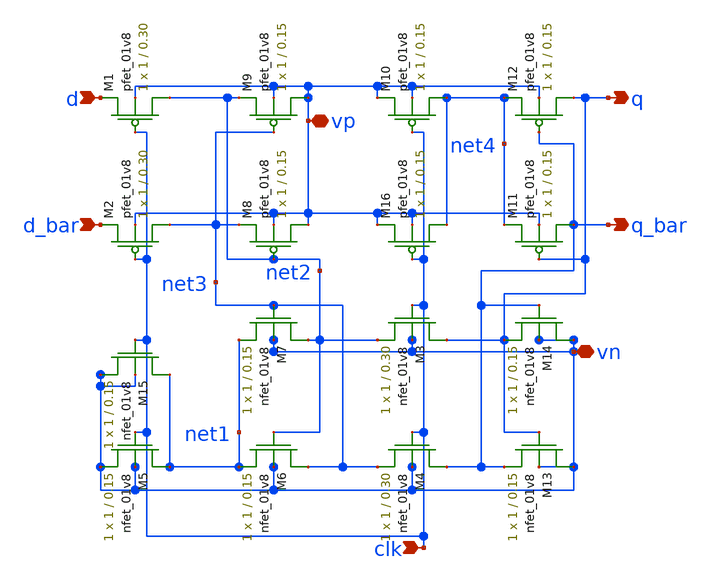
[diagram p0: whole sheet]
** sch_path: xschem/logic_gates/dflipflop.sch
**.subckt dflipflop q q_bar vp vn d_bar d clk
*.opin q
*.opin q_bar
*.iopin vp
*.iopin vn
*.ipin d_bar
*.ipin d
*.ipin clk
XM8 vp net2 net3 vp sky130_fd_pr__pfet_01v8 L=0.15 W=1 nf=1 ad='int((nf+1)/2) * W/nf * 0.29' as='int((nf+2)/2) * W/nf * 0.29'
+ pd='2*int((nf+1)/2) * (W/nf + 0.29)' ps='2*int((nf+2)/2) * (W/nf + 0.29)' nrd='0.29 / W' nrs='0.29 / W'
+ sa=0 sb=0 sd=0 mult=1 m=1
XM9 vp net3 net2 vp sky130_fd_pr__pfet_01v8 L=0.15 W=1 nf=1 ad='int((nf+1)/2) * W/nf * 0.29' as='int((nf+2)/2) * W/nf * 0.29'
+ pd='2*int((nf+1)/2) * (W/nf + 0.29)' ps='2*int((nf+2)/2) * (W/nf + 0.29)' nrd='0.29 / W' nrs='0.29 / W'
+ sa=0 sb=0 sd=0 mult=1 m=1
XM5 net1 clk vn vn sky130_fd_pr__nfet_01v8 L=0.15 W=1 nf=1 ad='int((nf+1)/2) * W/nf * 0.29' as='int((nf+2)/2) * W/nf * 0.29'
+ pd='2*int((nf+1)/2) * (W/nf + 0.29)' ps='2*int((nf+2)/2) * (W/nf + 0.29)' nrd='0.29 / W' nrs='0.29 / W'
+ sa=0 sb=0 sd=0 mult=1 m=1
XM6 net3 net2 net1 vn sky130_fd_pr__nfet_01v8 L=0.15 W=1 nf=1 ad='int((nf+1)/2) * W/nf * 0.29' as='int((nf+2)/2) * W/nf * 0.29'
+ pd='2*int((nf+1)/2) * (W/nf + 0.29)' ps='2*int((nf+2)/2) * (W/nf + 0.29)' nrd='0.29 / W' nrs='0.29 / W'
+ sa=0 sb=0 sd=0 mult=1 m=1
XM7 net2 net3 net1 vn sky130_fd_pr__nfet_01v8 L=0.15 W=1 nf=1 ad='int((nf+1)/2) * W/nf * 0.29' as='int((nf+2)/2) * W/nf * 0.29'
+ pd='2*int((nf+1)/2) * (W/nf + 0.29)' ps='2*int((nf+2)/2) * (W/nf + 0.29)' nrd='0.29 / W' nrs='0.29 / W'
+ sa=0 sb=0 sd=0 mult=1 m=1
XM13 vn q q_bar vn sky130_fd_pr__nfet_01v8 L=0.15 W=1 nf=1 ad='int((nf+1)/2) * W/nf * 0.29' as='int((nf+2)/2) * W/nf * 0.29'
+ pd='2*int((nf+1)/2) * (W/nf + 0.29)' ps='2*int((nf+2)/2) * (W/nf + 0.29)' nrd='0.29 / W' nrs='0.29 / W'
+ sa=0 sb=0 sd=0 mult=1 m=1
XM3 q clk net2 vn sky130_fd_pr__nfet_01v8 L=0.30 W=1 nf=1 ad='int((nf+1)/2) * W/nf * 0.29' as='int((nf+2)/2) * W/nf * 0.29'
+ pd='2*int((nf+1)/2) * (W/nf + 0.29)' ps='2*int((nf+2)/2) * (W/nf + 0.29)' nrd='0.29 / W' nrs='0.29 / W'
+ sa=0 sb=0 sd=0 mult=1 m=1
XM4 q_bar clk net3 vn sky130_fd_pr__nfet_01v8 L=0.30 W=1 nf=1 ad='int((nf+1)/2) * W/nf * 0.29' as='int((nf+2)/2) * W/nf * 0.29'
+ pd='2*int((nf+1)/2) * (W/nf + 0.29)' ps='2*int((nf+2)/2) * (W/nf + 0.29)' nrd='0.29 / W' nrs='0.29 / W'
+ sa=0 sb=0 sd=0 mult=1 m=1
XM14 vn q_bar q vn sky130_fd_pr__nfet_01v8 L=0.15 W=1 nf=1 ad='int((nf+1)/2) * W/nf * 0.29' as='int((nf+2)/2) * W/nf * 0.29'
+ pd='2*int((nf+1)/2) * (W/nf + 0.29)' ps='2*int((nf+2)/2) * (W/nf + 0.29)' nrd='0.29 / W' nrs='0.29 / W'
+ sa=0 sb=0 sd=0 mult=1 m=1
XM10 net4 clk vp vp sky130_fd_pr__pfet_01v8 L=0.15 W=1 nf=1 ad='int((nf+1)/2) * W/nf * 0.29' as='int((nf+2)/2) * W/nf * 0.29'
+ pd='2*int((nf+1)/2) * (W/nf + 0.29)' ps='2*int((nf+2)/2) * (W/nf + 0.29)' nrd='0.29 / W' nrs='0.29 / W'
+ sa=0 sb=0 sd=0 mult=1 m=1
XM11 q_bar q net4 vp sky130_fd_pr__pfet_01v8 L=0.15 W=1 nf=1 ad='int((nf+1)/2) * W/nf * 0.29' as='int((nf+2)/2) * W/nf * 0.29'
+ pd='2*int((nf+1)/2) * (W/nf + 0.29)' ps='2*int((nf+2)/2) * (W/nf + 0.29)' nrd='0.29 / W' nrs='0.29 / W'
+ sa=0 sb=0 sd=0 mult=1 m=1
XM12 q q_bar net4 vp sky130_fd_pr__pfet_01v8 L=0.15 W=1 nf=1 ad='int((nf+1)/2) * W/nf * 0.29' as='int((nf+2)/2) * W/nf * 0.29'
+ pd='2*int((nf+1)/2) * (W/nf + 0.29)' ps='2*int((nf+2)/2) * (W/nf + 0.29)' nrd='0.29 / W' nrs='0.29 / W'
+ sa=0 sb=0 sd=0 mult=1 m=1
XM15 net1 clk vn vn sky130_fd_pr__nfet_01v8 L=0.15 W=1 nf=1 ad='int((nf+1)/2) * W/nf * 0.29' as='int((nf+2)/2) * W/nf * 0.29'
+ pd='2*int((nf+1)/2) * (W/nf + 0.29)' ps='2*int((nf+2)/2) * (W/nf + 0.29)' nrd='0.29 / W' nrs='0.29 / W'
+ sa=0 sb=0 sd=0 mult=1 m=1
XM16 net4 clk vp vp sky130_fd_pr__pfet_01v8 L=0.15 W=1 nf=1 ad='int((nf+1)/2) * W/nf * 0.29' as='int((nf+2)/2) * W/nf * 0.29'
+ pd='2*int((nf+1)/2) * (W/nf + 0.29)' ps='2*int((nf+2)/2) * (W/nf + 0.29)' nrd='0.29 / W' nrs='0.29 / W'
+ sa=0 sb=0 sd=0 mult=1 m=1
XM1 net2 clk d vp sky130_fd_pr__pfet_01v8 L=0.30 W=1 nf=1 ad='int((nf+1)/2) * W/nf * 0.29' as='int((nf+2)/2) * W/nf * 0.29'
+ pd='2*int((nf+1)/2) * (W/nf + 0.29)' ps='2*int((nf+2)/2) * (W/nf + 0.29)' nrd='0.29 / W' nrs='0.29 / W'
+ sa=0 sb=0 sd=0 mult=1 m=1
XM2 net3 clk d_bar vp sky130_fd_pr__pfet_01v8 L=0.30 W=1 nf=1 ad='int((nf+1)/2) * W/nf * 0.29' as='int((nf+2)/2) * W/nf * 0.29'
+ pd='2*int((nf+1)/2) * (W/nf + 0.29)' ps='2*int((nf+2)/2) * (W/nf + 0.29)' nrd='0.29 / W' nrs='0.29 / W'
+ sa=0 sb=0 sd=0 mult=1 m=1
**.ends
.end
